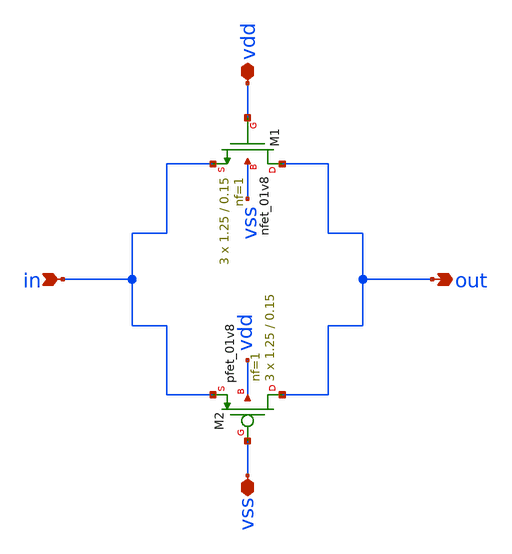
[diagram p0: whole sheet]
** sch_path: xschem/trans_gate.sch
**.subckt trans_gate vss in out vdd
*.iopin vss
*.ipin in
*.opin out
*.iopin vdd
XM2 out vss in vdd sky130_fd_pr__pfet_01v8 L=0.15 W=1.25 nf=1 ad='int((nf+1)/2) * W/nf * 0.29' as='int((nf+2)/2) * W/nf * 0.29'
+ pd='2*int((nf+1)/2) * (W/nf + 0.29)' ps='2*int((nf+2)/2) * (W/nf + 0.29)' nrd='0.29 / W' nrs='0.29 / W'
+ sa=0 sb=0 sd=0 mult=3 m=3
XM1 out vdd in vss sky130_fd_pr__nfet_01v8 L=0.15 W=1.25 nf=1 ad='int((nf+1)/2) * W/nf * 0.29' as='int((nf+2)/2) * W/nf * 0.29'
+ pd='2*int((nf+1)/2) * (W/nf + 0.29)' ps='2*int((nf+2)/2) * (W/nf + 0.29)' nrd='0.29 / W' nrs='0.29 / W'
+ sa=0 sb=0 sd=0 mult=3 m=3
**.ends
.end
